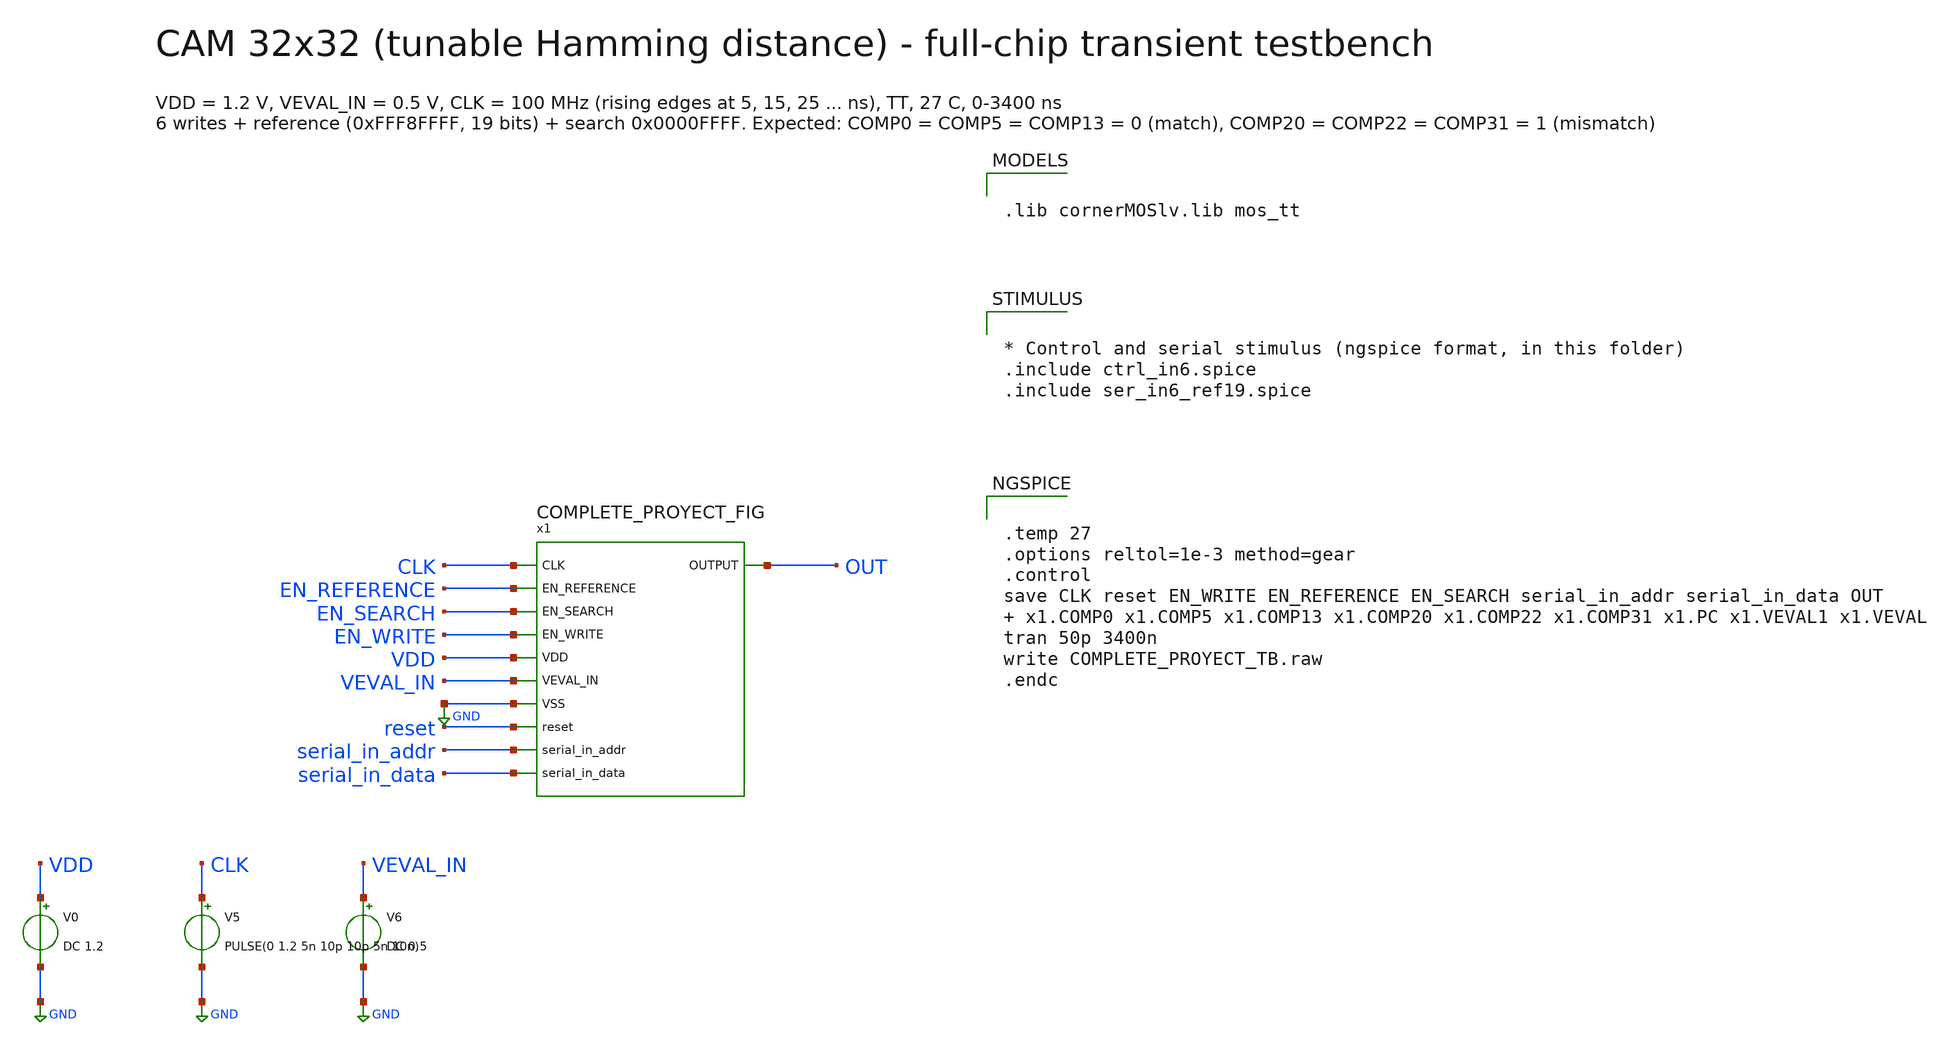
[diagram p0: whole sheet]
** sch_path: SoC6169-main/testbenches/tran/COMPLETE_PROYECT_TB.sch
* Copyright 2026 USFQ CAM team
* Licensed under the Apache License, Version 2.0 (the "License");
* you may not use this file except in compliance with the License.
* You may obtain a copy of the License at
* https://www.apache.org/licenses/LICENSE-2.0
* Unless required by applicable law or agreed to in writing, software
* distributed under the License is distributed on an "AS IS" BASIS,
* WITHOUT WARRANTIES OR CONDITIONS OF ANY KIND, either express or implied.
* See the License for the specific language governing permissions and
* limitations under the License.
**.subckt COMPLETE_PROYECT_TB
x1 CLK EN_REFERENCE EN_SEARCH EN_WRITE OUT VDD VEVAL_IN GND reset serial_in_addr serial_in_data
+ COMPLETE_PROYECT_FIG
V0 VDD GND DC 1.2
V5 CLK GND PULSE(0 1.2 5n 10p 10p 5n 10n)
V6 VEVAL_IN GND DC 0.5
**** begin user architecture code

.lib cornerMOSlv.lib mos_tt



* Control and serial stimulus (ngspice format, in this folder)
.include ctrl_in6.spice
.include ser_in6_ref19.spice




.temp 27
.options reltol=1e-3 method=gear
.control
save CLK reset EN_WRITE EN_REFERENCE EN_SEARCH serial_in_addr serial_in_data OUT  x1.COMP0 x1.COMP5
+ x1.COMP13 x1.COMP20 x1.COMP22 x1.COMP31 x1.PC x1.VEVAL1 x1.VEVAL
tran 50p 3400n
write COMPLETE_PROYECT_TB.raw
.endc


**** end user architecture code
**.ends
.GLOBAL GND
.end
